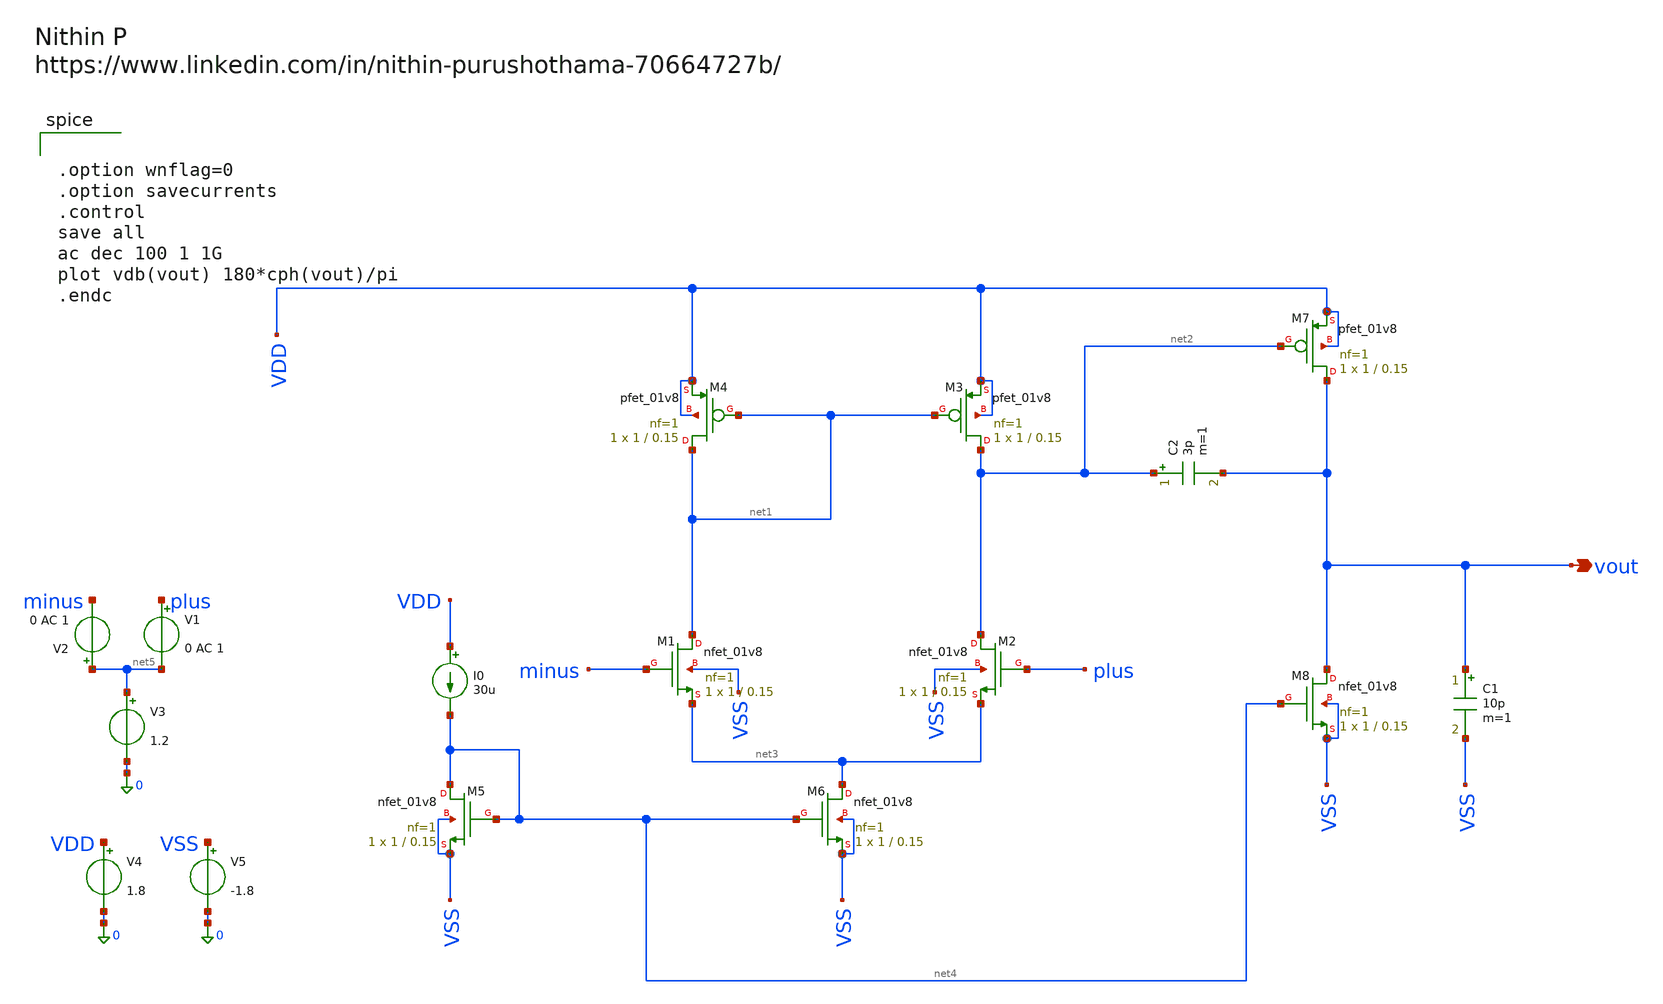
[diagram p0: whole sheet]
** sch_path: 2stageopamp.sch
**.subckt 2stageopamp vout
*.opin vout
C2 net2 vout 3p m=1
C1 vout VSS 10p m=1
XM1 net1 minus net3 VSS sky130_fd_pr__nfet_01v8 L=0.15 W=1 nf=1 ad='int((1 + 1)/2) * 1 / 1 * 0.29' as='int((1 + 2)/2) * 1 / 1 * 0.29'
+ pd='2*int((1 + 1)/2) * (1 / 1 + 0.29)' ps='2*int((1 + 2)/2) * (1 / 1 + 0.29)' nrd='0.29 / 1 ' nrs='0.29 / 1 '
+ sa=0 sb=0 sd=0 mult=1 m=1
XM2 net2 plus net3 VSS sky130_fd_pr__nfet_01v8 L=0.15 W=1 nf=1 ad='int((1 + 1)/2) * 1 / 1 * 0.29' as='int((1 + 2)/2) * 1 / 1 * 0.29'
+ pd='2*int((1 + 1)/2) * (1 / 1 + 0.29)' ps='2*int((1 + 2)/2) * (1 / 1 + 0.29)' nrd='0.29 / 1 ' nrs='0.29 / 1 '
+ sa=0 sb=0 sd=0 mult=1 m=1
XM3 net2 net1 VDD VDD sky130_fd_pr__pfet_01v8 L=0.15 W=1 nf=1 ad='int((1 + 1)/2) * 1 / 1 * 0.29' as='int((1 + 2)/2) * 1 / 1 * 0.29'
+ pd='2*int((1 + 1)/2) * (1 / 1 + 0.29)' ps='2*int((1 + 2)/2) * (1 / 1 + 0.29)' nrd='0.29 / 1 ' nrs='0.29 / 1 '
+ sa=0 sb=0 sd=0 mult=1 m=1
XM4 net1 net1 VDD VDD sky130_fd_pr__pfet_01v8 L=0.15 W=1 nf=1 ad='int((1 + 1)/2) * 1 / 1 * 0.29' as='int((1 + 2)/2) * 1 / 1 * 0.29'
+ pd='2*int((1 + 1)/2) * (1 / 1 + 0.29)' ps='2*int((1 + 2)/2) * (1 / 1 + 0.29)' nrd='0.29 / 1 ' nrs='0.29 / 1 '
+ sa=0 sb=0 sd=0 mult=1 m=1
XM5 net4 net4 VSS VSS sky130_fd_pr__nfet_01v8 L=0.15 W=1 nf=1 ad='int((1 + 1)/2) * 1 / 1 * 0.29' as='int((1 + 2)/2) * 1 / 1 * 0.29'
+ pd='2*int((1 + 1)/2) * (1 / 1 + 0.29)' ps='2*int((1 + 2)/2) * (1 / 1 + 0.29)' nrd='0.29 / 1 ' nrs='0.29 / 1 '
+ sa=0 sb=0 sd=0 mult=1 m=1
XM6 net3 net4 VSS VSS sky130_fd_pr__nfet_01v8 L=0.15 W=1 nf=1 ad='int((1 + 1)/2) * 1 / 1 * 0.29' as='int((1 + 2)/2) * 1 / 1 * 0.29'
+ pd='2*int((1 + 1)/2) * (1 / 1 + 0.29)' ps='2*int((1 + 2)/2) * (1 / 1 + 0.29)' nrd='0.29 / 1 ' nrs='0.29 / 1 '
+ sa=0 sb=0 sd=0 mult=1 m=1
XM7 vout net2 VDD VDD sky130_fd_pr__pfet_01v8 L=0.15 W=1 nf=1 ad='int((1 + 1)/2) * 1 / 1 * 0.29' as='int((1 + 2)/2) * 1 / 1 * 0.29'
+ pd='2*int((1 + 1)/2) * (1 / 1 + 0.29)' ps='2*int((1 + 2)/2) * (1 / 1 + 0.29)' nrd='0.29 / 1 ' nrs='0.29 / 1 '
+ sa=0 sb=0 sd=0 mult=1 m=1
XM8 vout net4 VSS VSS sky130_fd_pr__nfet_01v8 L=0.15 W=1 nf=1 ad='int((1 + 1)/2) * 1 / 1 * 0.29' as='int((1 + 2)/2) * 1 / 1 * 0.29'
+ pd='2*int((1 + 1)/2) * (1 / 1 + 0.29)' ps='2*int((1 + 2)/2) * (1 / 1 + 0.29)' nrd='0.29 / 1 ' nrs='0.29 / 1 '
+ sa=0 sb=0 sd=0 mult=1 m=1
I0 VDD net4 30u
V1 plus net5 0 AC 1
V2 net5 minus 0 AC 1
V3 net5 0 1.2
V4 VDD 0 1.8
V5 VSS 0 -1.8
**** begin user architecture code


.option wnflag=0
.option savecurrents
.control
save all
ac dec 100 1 1G
plot vdb(vout) 180*cph(vout)/pi
.endc



 .lib /foss/pdks/sky130A/libs.tech/ngspice/sky130.lib.spice tt

.param mc_mm_switch=0
.param mc_pr_switch=1

**** end user architecture code
**.ends
.end
